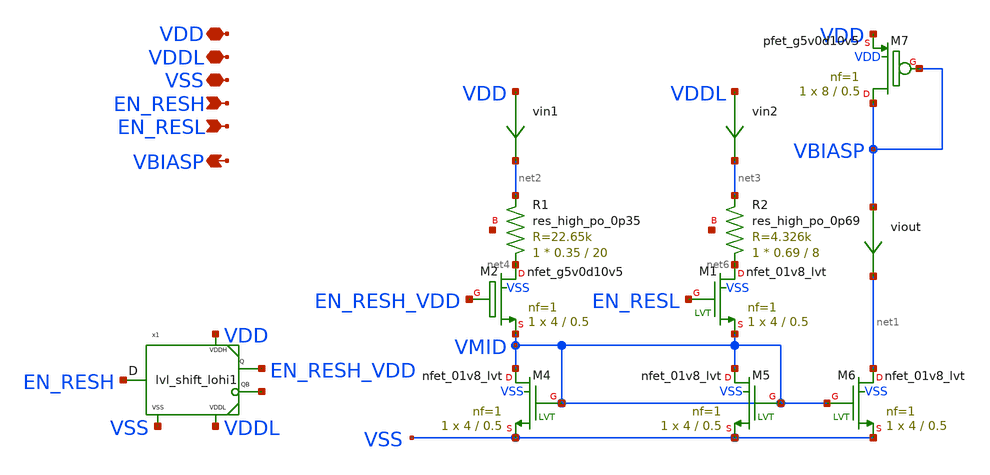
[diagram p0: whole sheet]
** sch_path: xschem/root_currents1.sch
**.subckt root_currents1 VSS EN_RESH VBIASP VDDL VDD EN_RESL
*.iopin VSS
*.ipin EN_RESH
*.opin VBIASP
*.iopin VDDL
*.iopin VDD
*.ipin EN_RESL
XR1 net4 net2 net5 sky130_fd_pr__res_high_po_0p35 L=20 mult=1 m=1
XR2 net6 net3 net7 sky130_fd_pr__res_high_po_0p69 L=8 mult=1 m=1
XM4 VMID VMID VSS VSS sky130_fd_pr__nfet_01v8_lvt L=0.5 W=4 nf=1 ad='int((nf+1)/2) * W/nf * 0.29' as='int((nf+2)/2) * W/nf * 0.29'
+ pd='2*int((nf+1)/2) * (W/nf + 0.29)' ps='2*int((nf+2)/2) * (W/nf + 0.29)' nrd='0.29 / W' nrs='0.29 / W'
+ sa=0 sb=0 sd=0 mult=1 m=1
XM5 VMID VMID VSS VSS sky130_fd_pr__nfet_01v8_lvt L=0.5 W=4 nf=1 ad='int((nf+1)/2) * W/nf * 0.29' as='int((nf+2)/2) * W/nf * 0.29'
+ pd='2*int((nf+1)/2) * (W/nf + 0.29)' ps='2*int((nf+2)/2) * (W/nf + 0.29)' nrd='0.29 / W' nrs='0.29 / W'
+ sa=0 sb=0 sd=0 mult=1 m=1
XM6 net1 VMID VSS VSS sky130_fd_pr__nfet_01v8_lvt L=0.5 W=4 nf=1 ad='int((nf+1)/2) * W/nf * 0.29' as='int((nf+2)/2) * W/nf * 0.29'
+ pd='2*int((nf+1)/2) * (W/nf + 0.29)' ps='2*int((nf+2)/2) * (W/nf + 0.29)' nrd='0.29 / W' nrs='0.29 / W'
+ sa=0 sb=0 sd=0 mult=1 m=1
XM2 net4 EN_RESH_VDD VMID VSS sky130_fd_pr__nfet_g5v0d10v5 L=0.5 W=4 nf=1 ad='int((nf+1)/2) * W/nf * 0.29'
+ as='int((nf+2)/2) * W/nf * 0.29' pd='2*int((nf+1)/2) * (W/nf + 0.29)' ps='2*int((nf+2)/2) * (W/nf + 0.29)'
+ nrd='0.29 / W' nrs='0.29 / W' sa=0 sb=0 sd=0 mult=1 m=1
viout VBIASP net1 0
.save i(viout)
x1 EN_RESH EN_RESH_VDD net8 VDD VDDL VSS lvl_shift_lohi1
XM7 VBIASP VBIASP VDD VDD sky130_fd_pr__pfet_g5v0d10v5 L=0.5 W=8 nf=1 ad='int((nf+1)/2) * W/nf * 0.29'
+ as='int((nf+2)/2) * W/nf * 0.29' pd='2*int((nf+1)/2) * (W/nf + 0.29)' ps='2*int((nf+2)/2) * (W/nf + 0.29)'
+ nrd='0.29 / W' nrs='0.29 / W' sa=0 sb=0 sd=0 mult=1 m=1
vin1 VDD net2 0
.save i(vin1)
vin2 VDDL net3 0
.save i(vin2)
XM1 net6 EN_RESL VMID VSS sky130_fd_pr__nfet_01v8_lvt L=0.5 W=4 nf=1 ad='int((nf+1)/2) * W/nf * 0.29'
+ as='int((nf+2)/2) * W/nf * 0.29' pd='2*int((nf+1)/2) * (W/nf + 0.29)' ps='2*int((nf+2)/2) * (W/nf + 0.29)'
+ nrd='0.29 / W' nrs='0.29 / W' sa=0 sb=0 sd=0 mult=1 m=1
**.ends

* expanding   symbol:  lvl_shift_lohi1.sym # of pins=6
** sym_path: xschem/lvl_shift_lohi1.sym
** sch_path: xschem/lvl_shift_lohi1.sch
.subckt lvl_shift_lohi1 D Q QB VDDH VDDL VSS
*.opin Q
*.ipin D
*.iopin VDDH
*.iopin VDDL
*.iopin VSS
*.opin QB
vpwr VDDL net1 0
.save i(vpwr)
XM1 QB Q VDDH VDDH sky130_fd_pr__pfet_g5v0d10v5 L=0.5 W=2 nf=1 ad='int((nf+1)/2) * W/nf * 0.29' as='int((nf+2)/2) * W/nf * 0.29'
+ pd='2*int((nf+1)/2) * (W/nf + 0.29)' ps='2*int((nf+2)/2) * (W/nf + 0.29)' nrd='0.29 / W' nrs='0.29 / W'
+ sa=0 sb=0 sd=0 mult=1 m=1
XM2 Q QB VDDH VDDH sky130_fd_pr__pfet_g5v0d10v5 L=0.5 W=2 nf=1 ad='int((nf+1)/2) * W/nf * 0.29' as='int((nf+2)/2) * W/nf * 0.29'
+ pd='2*int((nf+1)/2) * (W/nf + 0.29)' ps='2*int((nf+2)/2) * (W/nf + 0.29)' nrd='0.29 / W' nrs='0.29 / W'
+ sa=0 sb=0 sd=0 mult=1 m=1
XM3 QB D VSS VSS sky130_fd_pr__nfet_g5v0d10v5 L=0.5 W=4 nf=1 ad='int((nf+1)/2) * W/nf * 0.29' as='int((nf+2)/2) * W/nf * 0.29'
+ pd='2*int((nf+1)/2) * (W/nf + 0.29)' ps='2*int((nf+2)/2) * (W/nf + 0.29)' nrd='0.29 / W' nrs='0.29 / W'
+ sa=0 sb=0 sd=0 mult=1 m=1
XM4 Q DB VSS VSS sky130_fd_pr__nfet_g5v0d10v5 L=0.5 W=4 nf=1 ad='int((nf+1)/2) * W/nf * 0.29' as='int((nf+2)/2) * W/nf * 0.29'
+ pd='2*int((nf+1)/2) * (W/nf + 0.29)' ps='2*int((nf+2)/2) * (W/nf + 0.29)' nrd='0.29 / W' nrs='0.29 / W'
+ sa=0 sb=0 sd=0 mult=1 m=1
XM5 DB D VSS VSS sky130_fd_pr__nfet_01v8_lvt L=0.5 W=1 nf=1 ad='int((nf+1)/2) * W/nf * 0.29' as='int((nf+2)/2) * W/nf * 0.29'
+ pd='2*int((nf+1)/2) * (W/nf + 0.29)' ps='2*int((nf+2)/2) * (W/nf + 0.29)' nrd='0.29 / W' nrs='0.29 / W'
+ sa=0 sb=0 sd=0 mult=1 m=1
XM6 DB D net1 VDDL sky130_fd_pr__pfet_01v8_lvt L=0.5 W=2 nf=1 ad='int((nf+1)/2) * W/nf * 0.29' as='int((nf+2)/2) * W/nf * 0.29'
+ pd='2*int((nf+1)/2) * (W/nf + 0.29)' ps='2*int((nf+2)/2) * (W/nf + 0.29)' nrd='0.29 / W' nrs='0.29 / W'
+ sa=0 sb=0 sd=0 mult=1 m=1
.ends

.end
